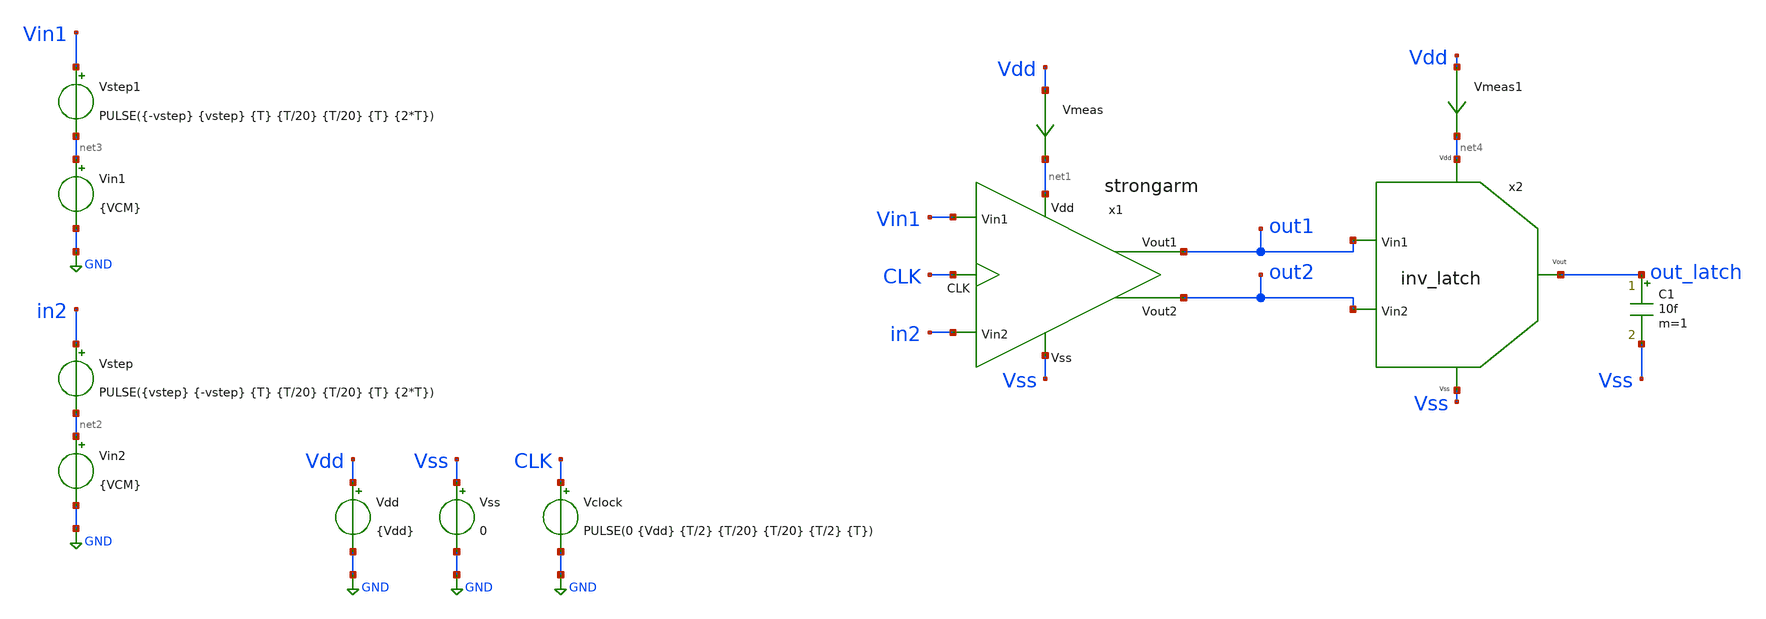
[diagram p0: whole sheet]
** sch_path: xschem/TB/TB_Tran_SA.sch
**.subckt TB_Tran_SA
Vdd Vdd GND {Vdd}
x1 out2 out1 net1 Vss in2 Vin1 CLK strongarm
Vss Vss GND 0
Vin1 net3 GND {VCM}
Vin2 net2 GND {VCM}
Vclock CLK GND PULSE(0 {Vdd} {T/2} {T/20} {T/20} {T/2} {T})
Vstep in2 net2 PULSE({vstep} {-vstep} {T} {T/20} {T/20} {T} {2*T})
Vmeas Vdd net1 0
.save i(vmeas)
Vstep1 Vin1 net3 PULSE({-vstep} {vstep} {T} {T/20} {T/20} {T} {2*T})
x2 net4 out_latch Vss out1 out2 inv_latch
Vmeas1 Vdd net4 0
.save i(vmeas1)
C1 out_latch Vss 10f m=1
**** begin user architecture code


.param Vdd   = 1.8
.param VCM   = 0.9
.param Vstep = 0.9
*.param Vstep = 0.5m
.param Vin2  = VCM
.ic V(out1) = 1.8
.ic V(out2) = 1.8
.ic V(x1.common) = 1.8
.ic V(x1.P) = 1.8
.ic V(x1.Q) = 1.8





.lib cornerMOSlv.lib mos_tt




.param T = 400p
.control
save all  @n.x1.xm3.nsg13_lv_nmos[vgs]  @n.x1.xm4.nsg13_lv_nmos[vgs]  @n.x1.xm5.nsg13_lv_pmos[vgs]
+  @n.x1.xm6.nsg13_lv_pmos[vgs]  @n.x1.xm10.nsg13_lv_pmos[vgs]  @n.x1.xm11.nsg13_lv_pmos[vgs]
*  @n.x1.xm10.nsg13_lv_pmos[vgt]  @n.x1.xm10.nsg13_lv_pmos[vth]  @n.x1.xm7.nsg13_lv_nmos[vds]
*  @n.x1.xm1.nsg13_lv_nmos[ids]  @n.x1.xm2.nsg13_lv_nmos[ids]  @n.x1.xm3.nsg13_lv_nmos[ids]
*+  @n.x1.xm4.nsg13_lv_nmos[ids]  @n.x1.xm5.nsg13_lv_pmos[ids]  @n.x1.xm6.nsg13_lv_pmos[ids]  @n.x1.xm7.nsg13_lv_nmos[ids]
*+  @n.x1.xm8.nsg13_lv_pmos[ids]  @n.x1.xm9.nsg13_lv_pmos[ids]  @n.x1.xm10.nsg13_lv_pmos[ids]  @n.x1.xm11.nsg13_lv_pmos[ids]
*  @n.x1.xm1.nsg13_lv_nmos[gds]  @n.x1.xm2.nsg13_lv_nmos[gds]  @n.x1.xm7.nsg13_lv_nmos[gds]

tran 0.1p 2n
let vgs3 = @n.x1.xm3.nsg13_lv_nmos[vgs]
let vgs4 = @n.x1.xm4.nsg13_lv_nmos[vgs]
let vgs5 = @n.x1.xm5.nsg13_lv_pmos[vgs]
let vgs6 = @n.x1.xm6.nsg13_lv_pmos[vgs]
let vgsa = @n.x1.xm10.nsg13_lv_pmos[vgs]
let vgsb = @n.x1.xm11.nsg13_lv_pmos[vgs]

let vgta = @n.x1.xm10.nsg13_lv_pmos[vgt]
let vtha = @n.x1.xm10.nsg13_lv_pmos[vth]

let id1 = @n.x1.xm1.nsg13_lv_nmos[ids]
let id2 = @n.x1.xm2.nsg13_lv_nmos[ids]
let id3 = @n.x1.xm3.nsg13_lv_nmos[ids]
let id4 = @n.x1.xm4.nsg13_lv_nmos[ids]
let id5 = @n.x1.xm5.nsg13_lv_pmos[ids]
let id6 = @n.x1.xm6.nsg13_lv_pmos[ids]
let id7 = @n.x1.xm7.nsg13_lv_nmos[ids]
let id8 = @n.x1.xm8.nsg13_lv_pmos[ids]
let id9 = @n.x1.xm9.nsg13_lv_pmos[ids]
let id10 = @n.x1.xm10.nsg13_lv_pmos[ids]
let id11 = @n.x1.xm11.nsg13_lv_pmos[ids]
let i_tot = i(vmeas)

let rds1 = 1/@n.x1.xm1.nsg13_lv_nmos[gds]
let rds2 = 1/@n.x1.xm2.nsg13_lv_nmos[gds]
let rds7 = 1/@n.x1.xm7.nsg13_lv_nmos[gds]
let Pot_SA = i_tot*v(vdd)
let Pot_SR = i(Vmeas1)*v(vdd)

meas tran id_peak1 MAX id1 from=200p to=600p
meas tran id_peak2 MAX id2 from=200p to=600p
meas tran id_peak3 MAX id3 from=200p to=600p
meas tran id_peak4 MAX id4 from=200p to=600p
meas tran id_peak5 MAX id5 from=200p to=600p
meas tran id_peak6 MAX id6 from=200p to=600p
meas tran id_peak7 MAX id7 from=200p to=400p
meas tran id_peak8 MAX id8 from=200p to=600p
meas tran id_peak9 MAX id9 from=200p to=600p
meas tran id_peak10 MAX id10 from=200p to=600p
meas tran id_peak11 MAX id11 from=200p to=600p
meas tran itot_max MAX i_tot from=200p to=600p

meas tran id_avg1 AVG id1 from=200p to=600p
meas tran id_avg2 AVG id2 from=200p to=600p
meas tran id_avg3 AVG id3 from=400p to=600p
meas tran id_avg4 AVG id4 from=200p to=400p
meas tran id_avg5 AVG id5 from=200p to=600p
meas tran id_avg6 AVG id6 from=200p to=600p
meas tran id_avg7 AVG id7 from=200p to=400p
meas tran id_avg8 AVG id8 from=400p to=600p
meas tran id_avg9 AVG id9 from=400p to=600p
meas tran id_avg10 AVG id10 from=400p to=600p
meas tran id_avg11 AVG id11 from=400p to=600p
meas tran itot_avg AVG i_tot from=200p to=600p

meas tran Amp_t TRIG AT=200p TARG v(out2) VAL=0.9 CROSS=1
meas tran reg_t TRIG v(out2) VAL=0.9  CROSS=1 TARG v(out2) VAL=0.01 CROSS=1
meas tran tp_lh TRIG v(clk) VAL=0.9 RISE=2 TARG v(out_latch) VAL=0.9 RISE=1
meas tran tp_hl TRIG v(clk) VAL=0.9 RISE=3 TARG v(out_latch) VAL=0.9 FALL=2
meas tran Avg_Power AVG Pot_SA from=200p to=600p
meas tran Avg_SR_pot AVG POT_SR from=200p to=600p
*meas tran Energy INTEG Pot from=200p to=400p
meas tran Energy INTEG Pot_SA from=200p to=600p
* se mide de dos manetas la energía en medio ciclo y ciclo entero

let tp = (tp_lh+tp_hl)/2
print tp
wrdata ../proyecto-IPD413/simulations/SA_tran_currents.raw id1 id2 id3 id4 id5 id6 id7 id8 id9 id10
+ id11
wrdata ../proyecto-IPD413/simulations/SA_tran_voltages.raw v(out1) v(out2) v(x1.P) x(x1.Q)
plot v(Vin1) v(in2)
plot v(out1) v(out2) v(clk)+2
plot v(clk) v(out_latch)
.endc




** TRANSISTORES NMOS

.param W12 = 2.5u
.param L12 = 0.5u
.param M12 = 8
.param F12 = 5

.param W34 = 2u
.param L34 = 0.13u
.param M34 = 4
.param F34 = 2

.param W56 = 3.5u
.param L56 = 0.13u
.param M56 = 1
.param F56 = 7

.param W7  = 1u
.param L7  = 0.13u
.param M7  = 15
.param F7  = 1

.param W89 = 1u
.param L89 = 0.13u
.param M89 = 2
.param F89 = 1

.param Wab = 0.7u
.param Lab = 0.13u
.param Mab = 4
.param Fab = 1


**** end user architecture code
**.ends

* expanding   symbol:  proyecto-IPD413/xschem/sch/strongarm.sym # of pins=7
** sym_path: xschem/sch/strongarm.sym
** sch_path: xschem/sch/strongarm.sch
.subckt strongarm Vout2 Vout1 Vdd Vss Vin2 Vin1 CLK
*.opin Vout2
*.opin Vout1
*.ipin Vin1
*.ipin Vin2
*.ipin CLK
*.ipin Vss
*.ipin Vdd
XM1 common Vin1 P Vss sg13_lv_nmos w={W12} l={L12} ng={F12} m={M12} mm_ok=1
XM2 common Vin2 Q Vss sg13_lv_nmos w={W12} l={L12} ng={F12} m={M12} mm_ok=1
XM3 P Vout2 Vout1 Vss sg13_lv_nmos w={W34} l={L34} ng={F34} m={M34} mm_ok=1
XM4 Q Vout1 Vout2 Vss sg13_lv_nmos w={W34} l={L34} ng={F34} m={M34} mm_ok=1
XM6 Vout2 Vout1 Vdd Vdd sg13_lv_pmos w={W56} l={L56} ng={F56} m={M56} mm_ok=1
XM5 Vout1 Vout2 Vdd Vdd sg13_lv_pmos w={W56} l={L56} ng={F56} m={M56} mm_ok=1
XM7 Vss CLK common Vss sg13_lv_nmos w={W7} l={L7} ng={F7} m={M7} mm_ok=1
XM8 P CLK Vdd Vdd sg13_lv_pmos w={W89} l={L89} ng={F89} m={M89} mm_ok=1
XM9 Q CLK Vdd Vdd sg13_lv_pmos w={W89} l={L89} ng={F89} m={M89} mm_ok=1
XM11 Vdd CLK Vout2 Vdd sg13_lv_pmos w={Wab} l={Lab} ng={Fab} m={Mab} mm_ok=1
XM10 Vdd CLK Vout1 Vdd sg13_lv_pmos w={Wab} l={Lab} ng={Fab} m={Mab} mm_ok=1
.ends


* expanding   symbol:  proyecto-IPD413/xschem/sch/inv_latch.sym # of pins=5
** sym_path: xschem/sch/inv_latch.sym
** sch_path: xschem/sch/inv_latch.sch
.subckt inv_latch Vdd Vout Vss Vin1 Vin2
*.opin Vout
*.ipin Vdd
*.ipin Vdd
*.ipin Vin1
*.ipin Vss
*.ipin Vss
*.ipin Vdd
*.ipin Vss
*.ipin Vdd
*.ipin Vin2
*.ipin Vss
*.ipin Vss
x1 net1 Vout Vdd Vss inv_lv
x2 Vout net1 Vdd Vss inv_lv
XM1 net1 net2 Vss Vss sg13_lv_nmos w=1.5u l=0.13u ng=1 m=1 mm_ok=1
x3 Vin1 net2 Vdd Vss inv_lv
XM2 Vout net3 Vss Vss sg13_lv_nmos w=1.5u l=0.13u ng=1 m=1 mm_ok=1
x4 Vin2 net3 Vdd Vss inv_lv
.ends


* expanding   symbol:  proyecto-IPD413/xschem/sch/inv_lv.sym # of pins=4
** sym_path: xschem/sch/inv_lv.sym
** sch_path: xschem/sch/inv_lv.sch
.subckt inv_lv Vin Vout Vdd Vss
*.ipin Vdd
*.ipin Vss
*.ipin Vin
*.opin Vout
XM1 Vss Vin Vout Vss sg13_lv_nmos w=1u l=0.13u ng=1 m=1 mm_ok=1
XM2 Vout Vin Vdd Vdd sg13_lv_pmos w=2.3u l=0.13u ng=1 m=1 mm_ok=1
.ends

.GLOBAL GND
.end
